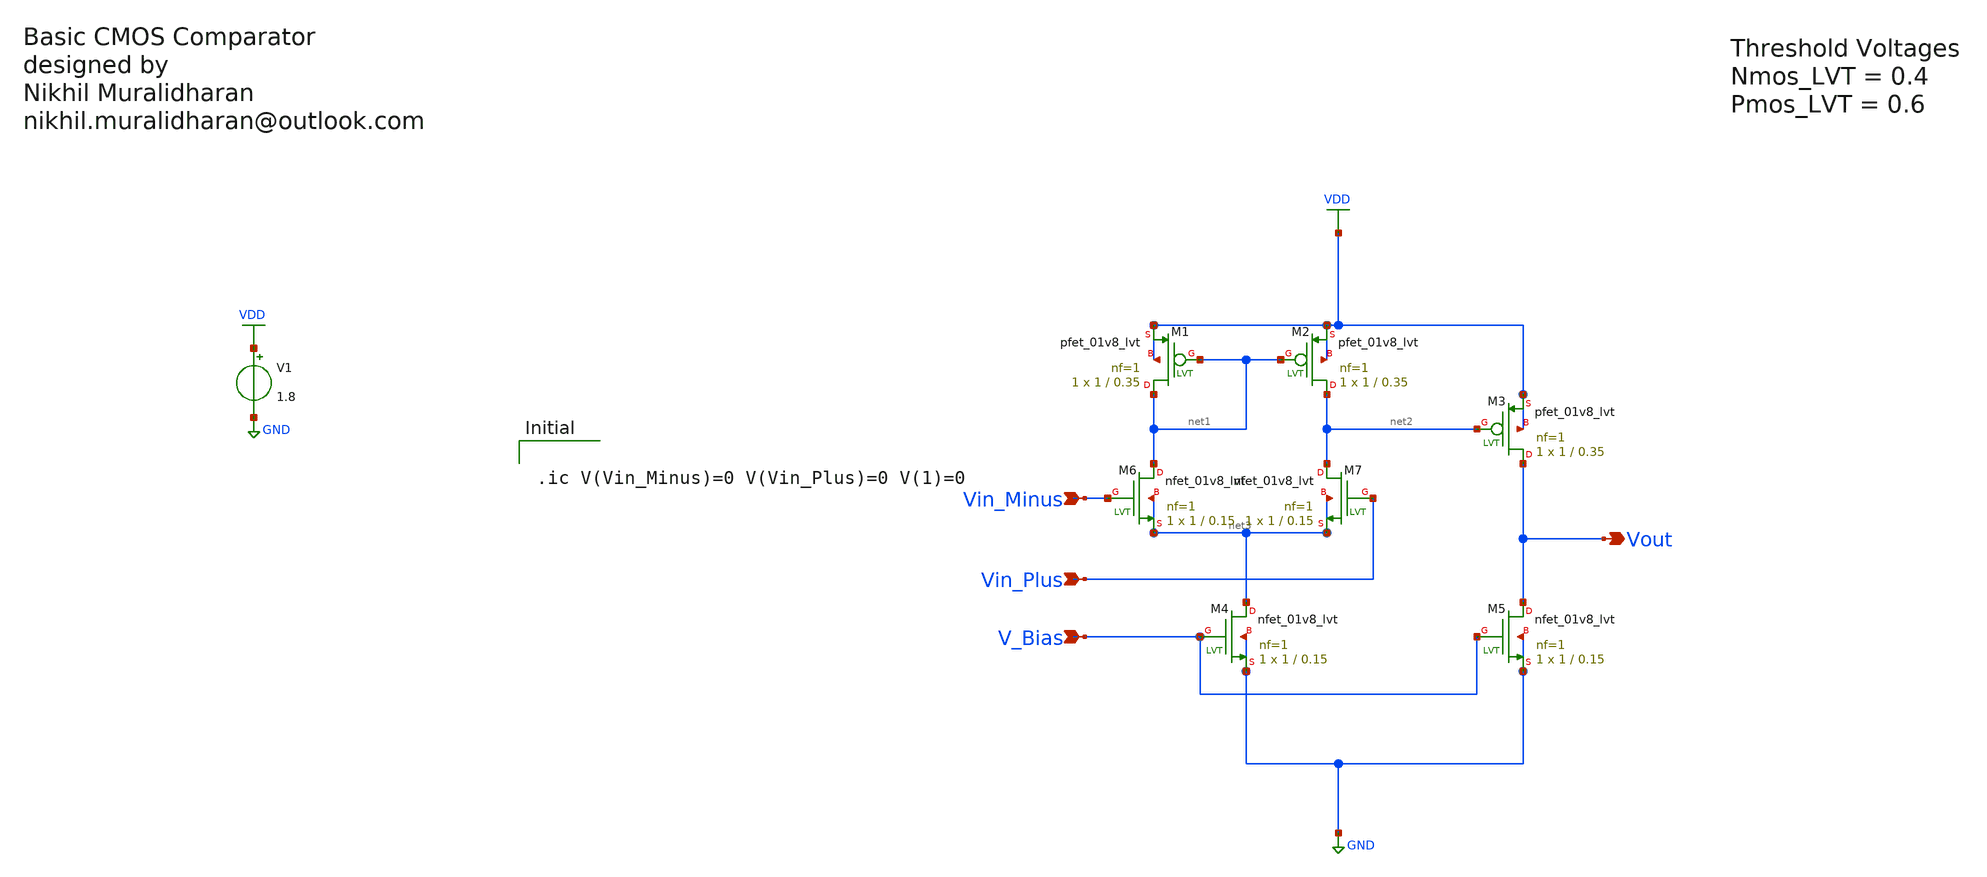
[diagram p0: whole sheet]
** sch_path: Current Sensor/Comparator.sch
**.subckt Comparator V_Bias Vin_Plus Vin_Minus Vout
*.ipin V_Bias
*.ipin Vin_Plus
*.ipin Vin_Minus
*.opin Vout
XM1 net1 net1 VDD VDD sky130_fd_pr__pfet_01v8_lvt L=0.35 W=1 nf=1 ad='int((nf+1)/2) * W/nf * 0.29' as='int((nf+2)/2) * W/nf * 0.29'
+ pd='2*int((nf+1)/2) * (W/nf + 0.29)' ps='2*int((nf+2)/2) * (W/nf + 0.29)' nrd='0.29 / W' nrs='0.29 / W'
+ sa=0 sb=0 sd=0 mult=1 m=1
XM2 net2 net1 VDD VDD sky130_fd_pr__pfet_01v8_lvt L=0.35 W=1 nf=1 ad='int((nf+1)/2) * W/nf * 0.29' as='int((nf+2)/2) * W/nf * 0.29'
+ pd='2*int((nf+1)/2) * (W/nf + 0.29)' ps='2*int((nf+2)/2) * (W/nf + 0.29)' nrd='0.29 / W' nrs='0.29 / W'
+ sa=0 sb=0 sd=0 mult=1 m=1
XM3 Vout net2 VDD VDD sky130_fd_pr__pfet_01v8_lvt L=0.35 W=1 nf=1 ad='int((nf+1)/2) * W/nf * 0.29' as='int((nf+2)/2) * W/nf * 0.29'
+ pd='2*int((nf+1)/2) * (W/nf + 0.29)' ps='2*int((nf+2)/2) * (W/nf + 0.29)' nrd='0.29 / W' nrs='0.29 / W'
+ sa=0 sb=0 sd=0 mult=1 m=1
XM4 net3 V_Bias GND GND sky130_fd_pr__nfet_01v8_lvt L=0.15 W=1 nf=1 ad='int((nf+1)/2) * W/nf * 0.29'
+ as='int((nf+2)/2) * W/nf * 0.29' pd='2*int((nf+1)/2) * (W/nf + 0.29)' ps='2*int((nf+2)/2) * (W/nf + 0.29)'
+ nrd='0.29 / W' nrs='0.29 / W' sa=0 sb=0 sd=0 mult=1 m=1
XM5 Vout V_Bias GND GND sky130_fd_pr__nfet_01v8_lvt L=0.15 W=1 nf=1 ad='int((nf+1)/2) * W/nf * 0.29'
+ as='int((nf+2)/2) * W/nf * 0.29' pd='2*int((nf+1)/2) * (W/nf + 0.29)' ps='2*int((nf+2)/2) * (W/nf + 0.29)'
+ nrd='0.29 / W' nrs='0.29 / W' sa=0 sb=0 sd=0 mult=1 m=1
XM6 net1 Vin_Minus net3 net3 sky130_fd_pr__nfet_01v8_lvt L=0.15 W=1 nf=1 ad='int((nf+1)/2) * W/nf * 0.29'
+ as='int((nf+2)/2) * W/nf * 0.29' pd='2*int((nf+1)/2) * (W/nf + 0.29)' ps='2*int((nf+2)/2) * (W/nf + 0.29)'
+ nrd='0.29 / W' nrs='0.29 / W' sa=0 sb=0 sd=0 mult=1 m=1
XM7 net2 Vin_Plus net3 net3 sky130_fd_pr__nfet_01v8_lvt L=0.15 W=1 nf=1 ad='int((nf+1)/2) * W/nf * 0.29'
+ as='int((nf+2)/2) * W/nf * 0.29' pd='2*int((nf+1)/2) * (W/nf + 0.29)' ps='2*int((nf+2)/2) * (W/nf + 0.29)'
+ nrd='0.29 / W' nrs='0.29 / W' sa=0 sb=0 sd=0 mult=1 m=1
V1 VDD GND 1.8
**** begin user architecture code


.ic V(Vin_Minus)=0 V(Vin_Plus)=0 V(1)=0


**** end user architecture code
**.ends
.GLOBAL VDD
.GLOBAL GND
.end
